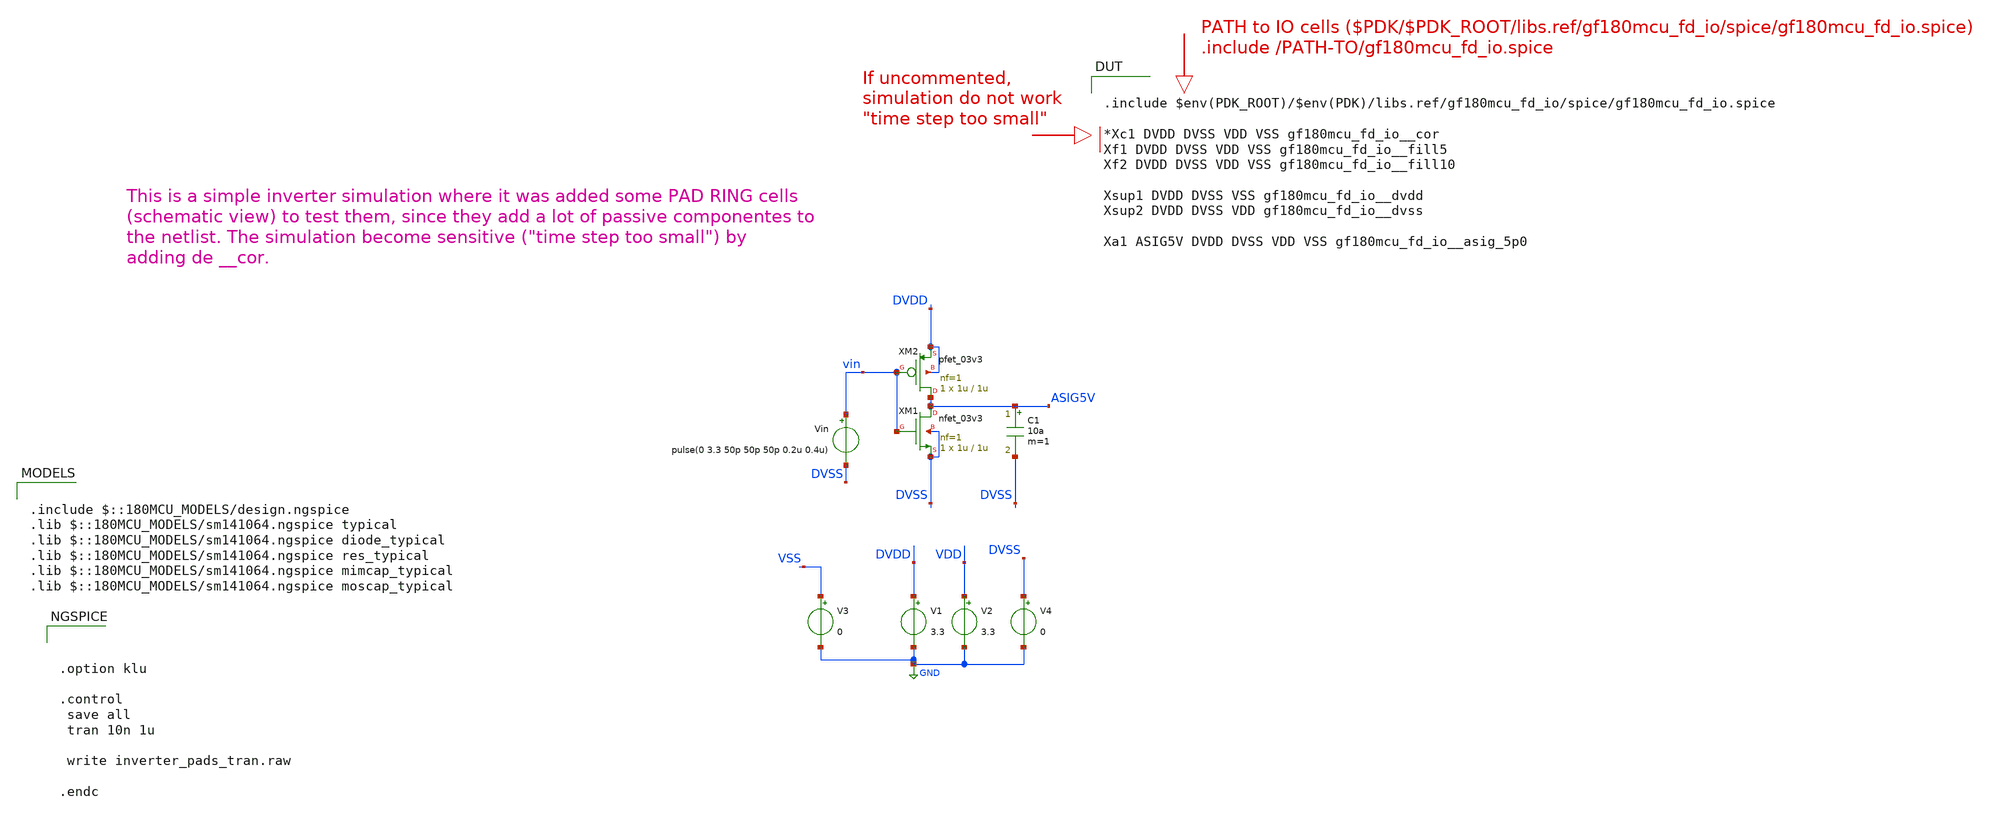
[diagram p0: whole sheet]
** sch_path: designs/Chipathon2025_pads/xschem/inverter_pads_tran.sch
**.subckt inverter_pads_tran
V1 DVDD GND 3.3
V2 VDD GND 3.3
Vin vin DVSS pulse(0 3.3 50p 50p 50p 0.2u 0.4u)
C1 ASIG5V DVSS 10a m=1
V3 VSS GND 0
V4 DVSS GND 0
XM1 ASIG5V vin DVSS DVSS nfet_03v3 L=1u W=1u nf=1 ad='int((nf+1)/2) * W/nf * 0.18u' as='int((nf+2)/2) * W/nf * 0.18u'
+ pd='2*int((nf+1)/2) * (W/nf + 0.18u)' ps='2*int((nf+2)/2) * (W/nf + 0.18u)' nrd='0.18u / W' nrs='0.18u / W'
+ sa=0 sb=0 sd=0 m=1
XM2 ASIG5V vin DVDD DVDD pfet_03v3 L=1u W=1u nf=1 ad='int((nf+1)/2) * W/nf * 0.18u' as='int((nf+2)/2) * W/nf * 0.18u'
+ pd='2*int((nf+1)/2) * (W/nf + 0.18u)' ps='2*int((nf+2)/2) * (W/nf + 0.18u)' nrd='0.18u / W' nrs='0.18u / W'
+ sa=0 sb=0 sd=0 m=1
**** begin user architecture code

.include $::180MCU_MODELS/design.ngspice
.lib $::180MCU_MODELS/sm141064.ngspice typical
.lib $::180MCU_MODELS/sm141064.ngspice diode_typical
.lib $::180MCU_MODELS/sm141064.ngspice res_typical
.lib $::180MCU_MODELS/sm141064.ngspice mimcap_typical
.lib $::180MCU_MODELS/sm141064.ngspice moscap_typical


.include $env(PDK_ROOT)/$env(PDK)/libs.ref/gf180mcu_fd_io/spice/gf180mcu_fd_io.spice

*Xc1 DVDD DVSS VDD VSS gf180mcu_fd_io__cor
Xf1 DVDD DVSS VDD VSS gf180mcu_fd_io__fill5
Xf2 DVDD DVSS VDD VSS gf180mcu_fd_io__fill10

Xsup1 DVDD DVSS VSS gf180mcu_fd_io__dvdd
Xsup2 DVDD DVSS VDD gf180mcu_fd_io__dvss

Xa1 ASIG5V DVDD DVSS VDD VSS gf180mcu_fd_io__asig_5p0





.option klu

.control
 save all
 tran 10n 1u

 write inverter_pads_tran.raw

.endc



**** end user architecture code
**.ends
.GLOBAL GND
.end
